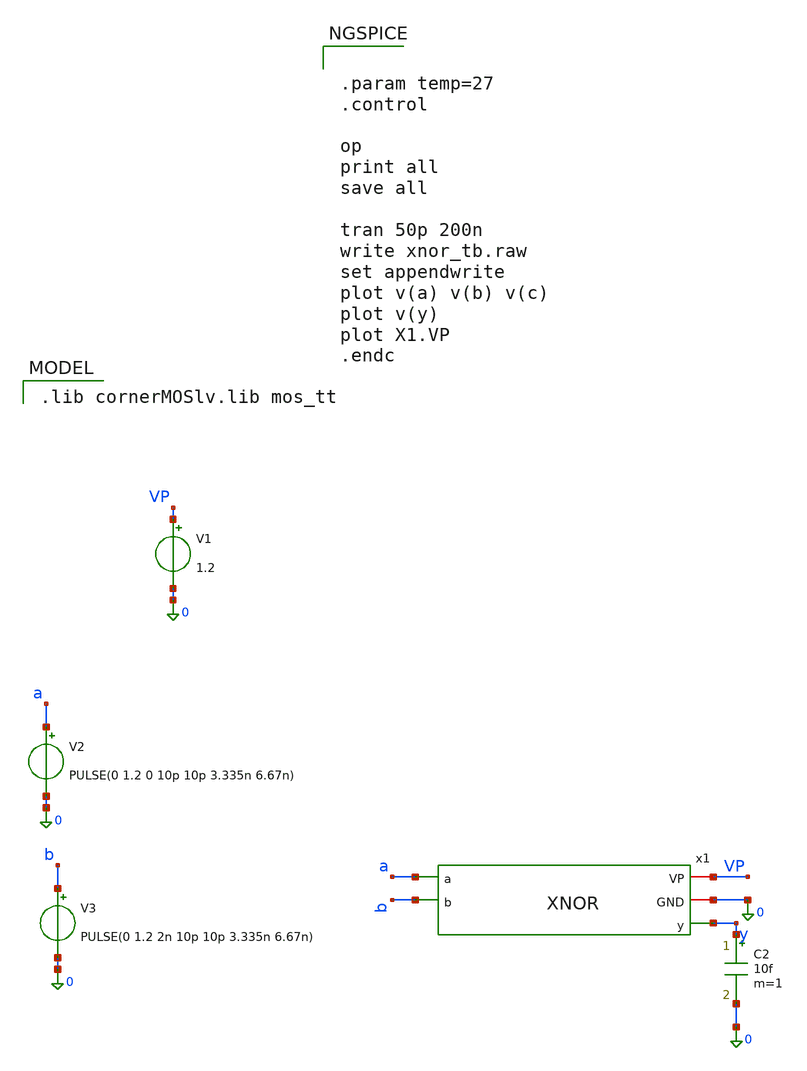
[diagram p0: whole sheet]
** sch_path: PLL0663-main/testbenches/tran/xschem/divider/xnor_tb.sch
**.subckt xnor_tb
V1 VP 0 1.2
V2 a 0 PULSE(0 1.2 0 10p 10p 3.335n 6.67n)
C2 y 0 10f m=1
x1 VP 0 a y b XNOR
V3 b 0 PULSE(0 1.2 2n 10p 10p 3.335n 6.67n)
**** begin user architecture code
 .lib cornerMOSlv.lib mos_tt



.param temp=27
.control

op
print all
save all

tran 50p 200n
write xnor_tb.raw
set appendwrite
plot v(a) v(b) v(c)
plot v(y)
plot X1.VP
.endc


**** end user architecture code
**.ends
.end
